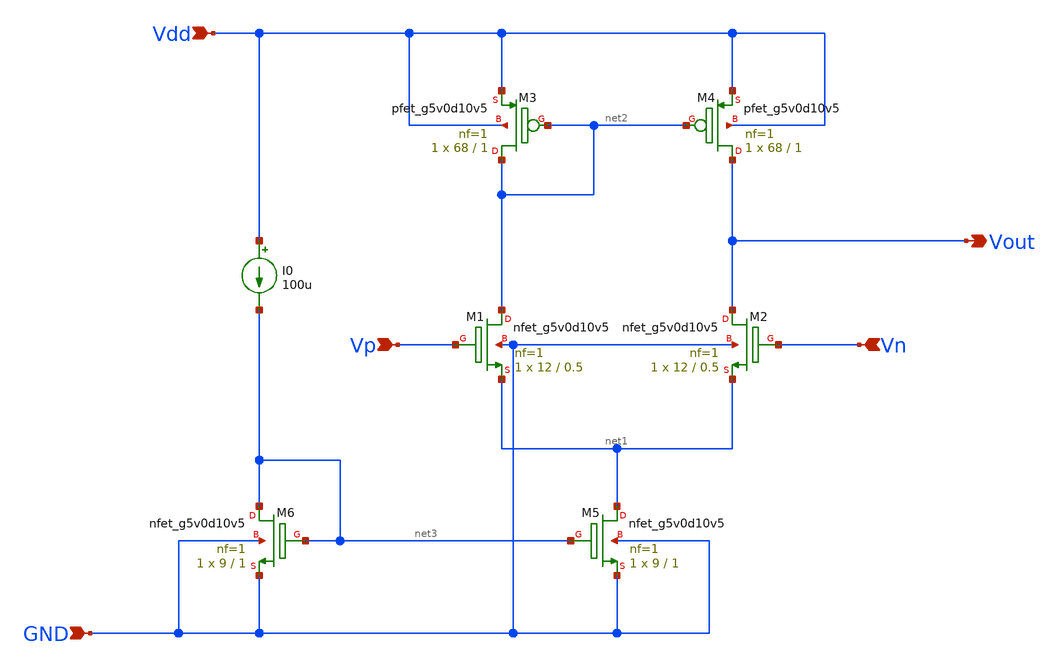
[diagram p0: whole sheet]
** sch_path: LDO/Schematic/Error_Amplifier.sch
**.subckt Error_Amplifier Vout Vdd GND Vn Vp
*.opin Vout
*.ipin Vdd
*.ipin GND
*.ipin Vn
*.ipin Vp
XM3 net2 net2 Vdd Vdd sky130_fd_pr__pfet_g5v0d10v5 L=1 W=68 nf=1 ad='int((nf+1)/2) * W/nf * 0.29' as='int((nf+2)/2) * W/nf * 0.29'
+ pd='2*int((nf+1)/2) * (W/nf + 0.29)' ps='2*int((nf+2)/2) * (W/nf + 0.29)' nrd='0.29 / W' nrs='0.29 / W'
+ sa=0 sb=0 sd=0 mult=1 m=1
XM4 Vout net2 Vdd Vdd sky130_fd_pr__pfet_g5v0d10v5 L=1 W=68 nf=1 ad='int((nf+1)/2) * W/nf * 0.29' as='int((nf+2)/2) * W/nf * 0.29'
+ pd='2*int((nf+1)/2) * (W/nf + 0.29)' ps='2*int((nf+2)/2) * (W/nf + 0.29)' nrd='0.29 / W' nrs='0.29 / W'
+ sa=0 sb=0 sd=0 mult=1 m=1
XM1 net2 Vp net1 GND sky130_fd_pr__nfet_g5v0d10v5 L=0.5 W=12 nf=1 ad='int((nf+1)/2) * W/nf * 0.29' as='int((nf+2)/2) * W/nf * 0.29'
+ pd='2*int((nf+1)/2) * (W/nf + 0.29)' ps='2*int((nf+2)/2) * (W/nf + 0.29)' nrd='0.29 / W' nrs='0.29 / W'
+ sa=0 sb=0 sd=0 mult=1 m=1
XM2 Vout Vn net1 GND sky130_fd_pr__nfet_g5v0d10v5 L=0.5 W=12 nf=1 ad='int((nf+1)/2) * W/nf * 0.29' as='int((nf+2)/2) * W/nf * 0.29'
+ pd='2*int((nf+1)/2) * (W/nf + 0.29)' ps='2*int((nf+2)/2) * (W/nf + 0.29)' nrd='0.29 / W' nrs='0.29 / W'
+ sa=0 sb=0 sd=0 mult=1 m=1
XM5 net1 net3 GND GND sky130_fd_pr__nfet_g5v0d10v5 L=1 W=9 nf=1 ad='int((nf+1)/2) * W/nf * 0.29' as='int((nf+2)/2) * W/nf * 0.29'
+ pd='2*int((nf+1)/2) * (W/nf + 0.29)' ps='2*int((nf+2)/2) * (W/nf + 0.29)' nrd='0.29 / W' nrs='0.29 / W'
+ sa=0 sb=0 sd=0 mult=1 m=1
XM6 net3 net3 GND GND sky130_fd_pr__nfet_g5v0d10v5 L=1 W=9 nf=1 ad='int((nf+1)/2) * W/nf * 0.29' as='int((nf+2)/2) * W/nf * 0.29'
+ pd='2*int((nf+1)/2) * (W/nf + 0.29)' ps='2*int((nf+2)/2) * (W/nf + 0.29)' nrd='0.29 / W' nrs='0.29 / W'
+ sa=0 sb=0 sd=0 mult=1 m=1
I0 Vdd net3 100u
**.ends
.end
